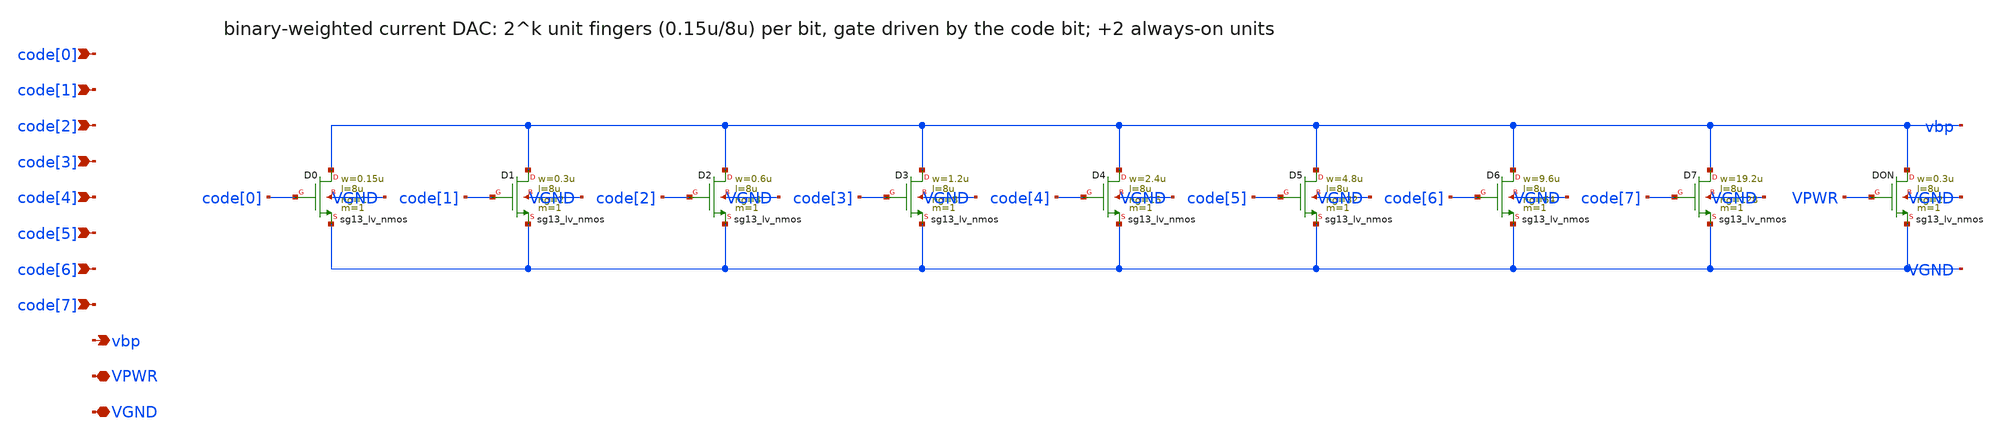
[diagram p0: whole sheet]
** sch_path: analog/xschem/csro_dac.sch
**.subckt csro_dac code[0] code[1] code[2] code[3] code[4] code[5] code[6] code[7] vbp VPWR VGND
*.ipin code[0]
*.ipin code[1]
*.ipin code[2]
*.ipin code[3]
*.ipin code[4]
*.ipin code[5]
*.ipin code[6]
*.ipin code[7]
*.opin vbp
*.iopin VPWR
*.iopin VGND
XD0 vbp code[0] VGND VGND sg13_lv_nmos w=0.15u l=8u ng=1 m=1 mm_ok=1
XD1 vbp code[1] VGND VGND sg13_lv_nmos w=0.3u l=8u ng=2 m=1 mm_ok=1
XD2 vbp code[2] VGND VGND sg13_lv_nmos w=0.6u l=8u ng=4 m=1 mm_ok=1
XD3 vbp code[3] VGND VGND sg13_lv_nmos w=1.2u l=8u ng=8 m=1 mm_ok=1
XD4 vbp code[4] VGND VGND sg13_lv_nmos w=2.4u l=8u ng=16 m=1 mm_ok=1
XD5 vbp code[5] VGND VGND sg13_lv_nmos w=4.8u l=8u ng=32 m=1 mm_ok=1
XD6 vbp code[6] VGND VGND sg13_lv_nmos w=9.6u l=8u ng=64 m=1 mm_ok=1
XD7 vbp code[7] VGND VGND sg13_lv_nmos w=19.2u l=8u ng=128 m=1 mm_ok=1
XDON vbp VPWR VGND VGND sg13_lv_nmos w=0.3u l=8u ng=2 m=1 mm_ok=1
**.ends
.end
